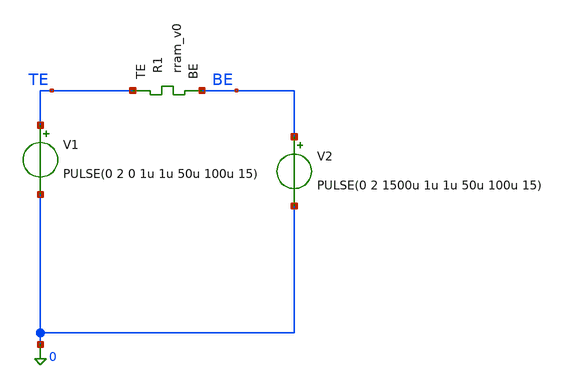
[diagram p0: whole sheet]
** sch_path: memristor_models/wellposed/tb_pulses_well.sch
**.subckt tb_pulses_well
V1 TE 0 PULSE(0 2 0 1u 1u 50u 100u 15)
V2 BE 0 PULSE(0 2 1500u 1u 1u 50u 100u 15)
XR1 TE BE rram_v0
**** begin user architecture code

** opencircuitdesign pdks install
.inc $::SKYWATER_MODELS/rram_v0.spice



.option savecurrents
.tran 1u 3m
.control
	save all
	run
	write tb_pulses_well.raw
.endc



**** end user architecture code
**.ends
.end
